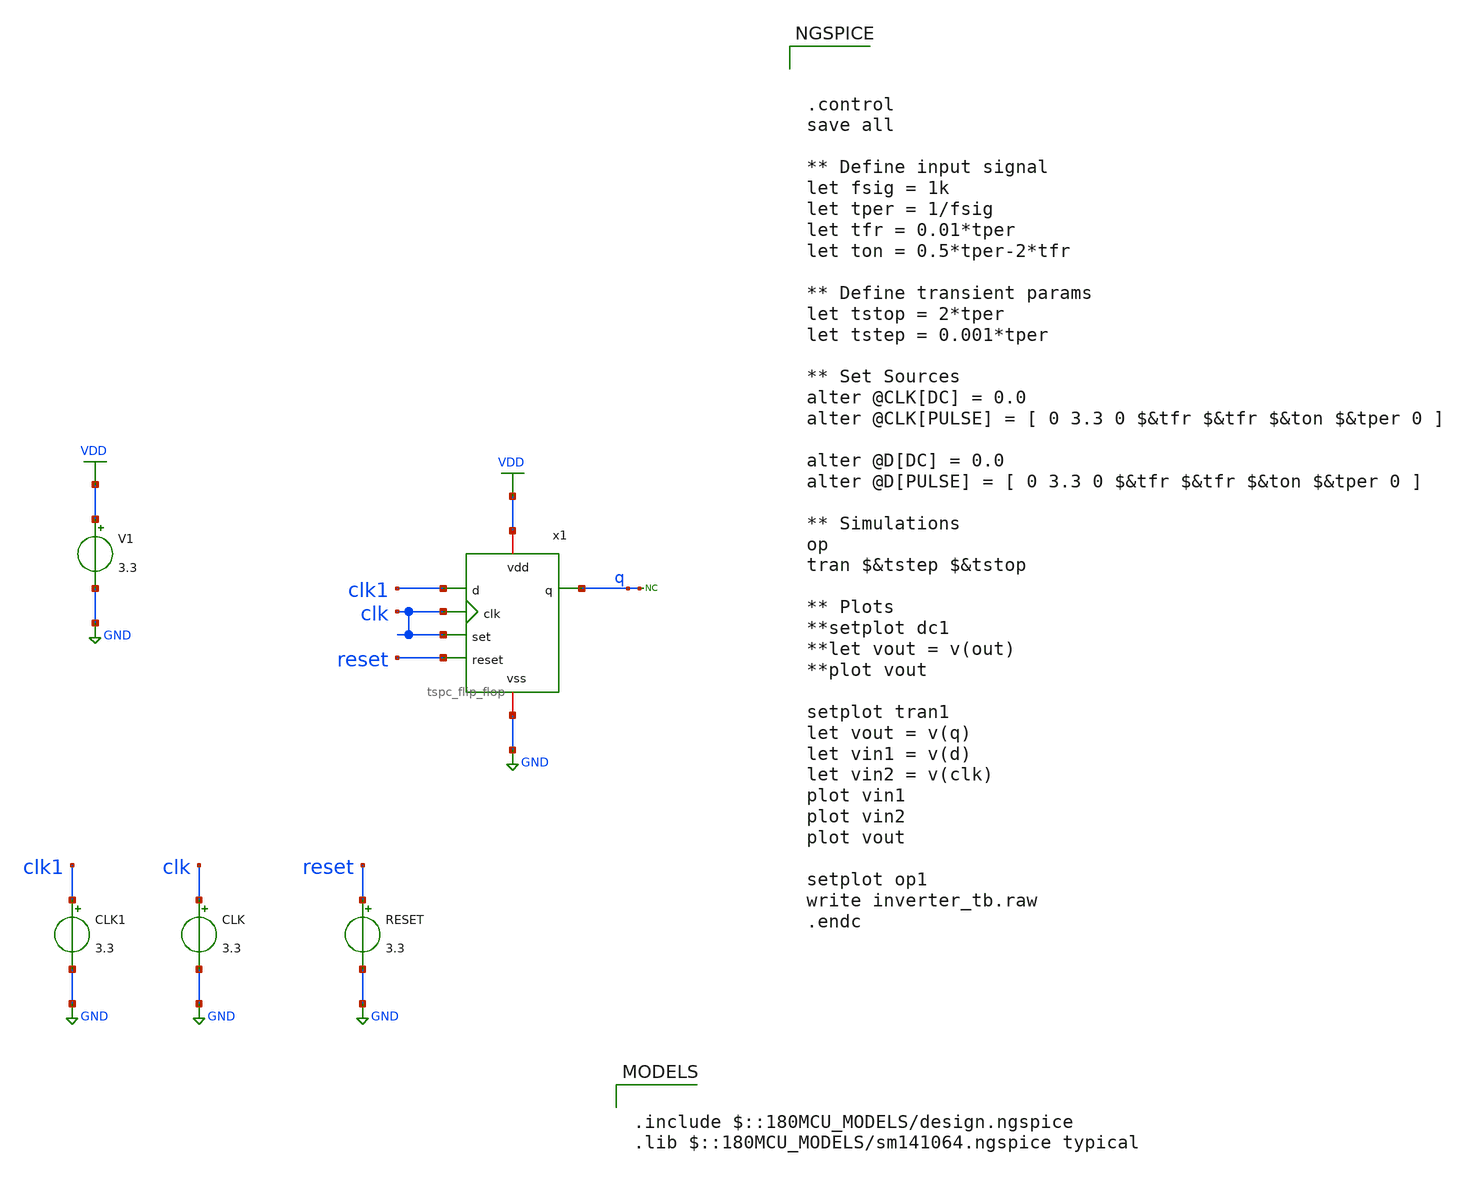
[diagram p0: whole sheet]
** sch_path: designs/libs/tspc_flip_flop/tspc_flip_flop_tb.sch
**.subckt tspc_flip_flop_tb
x1 VDD GND clk1 clk clk reset q tspc_flip_flop
V1 VDD GND 3.3
CLK clk GND 3.3
RESET reset GND 3.3
* noconn q
CLK1 clk1 GND 3.3
**** begin user architecture code

.include $::180MCU_MODELS/design.ngspice
.lib $::180MCU_MODELS/sm141064.ngspice typical




.control
save all

** Define input signal
let fsig = 1k
let tper = 1/fsig
let tfr = 0.01*tper
let ton = 0.5*tper-2*tfr

** Define transient params
let tstop = 2*tper
let tstep = 0.001*tper

** Set Sources
alter @CLK[DC] = 0.0
alter @CLK[PULSE] = [ 0 3.3 0 $&tfr $&tfr $&ton $&tper 0 ]

alter @D[DC] = 0.0
alter @D[PULSE] = [ 0 3.3 0 $&tfr $&tfr $&ton $&tper 0 ]

** Simulations
op
tran $&tstep $&tstop

** Plots
**setplot dc1
**let vout = v(out)
**plot vout

setplot tran1
let vout = v(q)
let vin1 = v(d)
let vin2 = v(clk)
plot vin1
plot vin2
plot vout

setplot op1
write inverter_tb.raw
.endc


**** end user architecture code
**.ends

* expanding   symbol:  libs/tspc_flip_flop/tspc_flip_flop.sym # of pins=7
** sym_path: designs/libs/tspc_flip_flop/tspc_flip_flop.sym
** sch_path: designs/libs/tspc_flip_flop/tspc_flip_flop.sch
.subckt tspc_flip_flop vdd vss d clk set reset q
*.iopin vdd
*.iopin vss
*.ipin d
*.ipin clk
*.ipin set
*.ipin reset
*.opin q
XM1 net2 d vss vss nfet_03v3 L=0.28u W=0.22u nf=1 ad='int((nf+1)/2) * W/nf * 0.18u' as='int((nf+2)/2) * W/nf * 0.18u'
+ pd='2*int((nf+1)/2) * (W/nf + 0.18u)' ps='2*int((nf+2)/2) * (W/nf + 0.18u)' nrd='0.18u / W' nrs='0.18u / W'
+ sa=0 sb=0 sd=0 m=1
XM2 net2 clk net1 net1 pfet_03v3 L=0.28u W=0.22u nf=1 ad='int((nf+1)/2) * W/nf * 0.18u' as='int((nf+2)/2) * W/nf * 0.18u'
+ pd='2*int((nf+1)/2) * (W/nf + 0.18u)' ps='2*int((nf+2)/2) * (W/nf + 0.18u)' nrd='0.18u / W' nrs='0.18u / W'
+ sa=0 sb=0 sd=0 m=1
XM3 net1 d vdd vdd pfet_03v3 L=0.28u W=0.22u nf=1 ad='int((nf+1)/2) * W/nf * 0.18u' as='int((nf+2)/2) * W/nf * 0.18u'
+ pd='2*int((nf+1)/2) * (W/nf + 0.18u)' ps='2*int((nf+2)/2) * (W/nf + 0.18u)' nrd='0.18u / W' nrs='0.18u / W'
+ sa=0 sb=0 sd=0 m=1
XM4 net3 clk vdd vdd pfet_03v3 L=0.28u W=0.22u nf=1 ad='int((nf+1)/2) * W/nf * 0.18u' as='int((nf+2)/2) * W/nf * 0.18u'
+ pd='2*int((nf+1)/2) * (W/nf + 0.18u)' ps='2*int((nf+2)/2) * (W/nf + 0.18u)' nrd='0.18u / W' nrs='0.18u / W'
+ sa=0 sb=0 sd=0 m=1
XM5 net3 net2 net4 vss nfet_03v3 L=0.28u W=0.22u nf=1 ad='int((nf+1)/2) * W/nf * 0.18u' as='int((nf+2)/2) * W/nf * 0.18u'
+ pd='2*int((nf+1)/2) * (W/nf + 0.18u)' ps='2*int((nf+2)/2) * (W/nf + 0.18u)' nrd='0.18u / W' nrs='0.18u / W'
+ sa=0 sb=0 sd=0 m=1
XM6 net4 clk vss vss nfet_03v3 L=0.28u W=0.22u nf=1 ad='int((nf+1)/2) * W/nf * 0.18u' as='int((nf+2)/2) * W/nf * 0.18u'
+ pd='2*int((nf+1)/2) * (W/nf + 0.18u)' ps='2*int((nf+2)/2) * (W/nf + 0.18u)' nrd='0.18u / W' nrs='0.18u / W'
+ sa=0 sb=0 sd=0 m=1
XM7 net7 net3 vss vss nfet_03v3 L=0.28u W=0.22u nf=1 ad='int((nf+1)/2) * W/nf * 0.18u' as='int((nf+2)/2) * W/nf * 0.18u'
+ pd='2*int((nf+1)/2) * (W/nf + 0.18u)' ps='2*int((nf+2)/2) * (W/nf + 0.18u)' nrd='0.18u / W' nrs='0.18u / W'
+ sa=0 sb=0 sd=0 m=1
XM8 net5 clk net7 vss nfet_03v3 L=0.28u W=0.22u nf=1 ad='int((nf+1)/2) * W/nf * 0.18u' as='int((nf+2)/2) * W/nf * 0.18u'
+ pd='2*int((nf+1)/2) * (W/nf + 0.18u)' ps='2*int((nf+2)/2) * (W/nf + 0.18u)' nrd='0.18u / W' nrs='0.18u / W'
+ sa=0 sb=0 sd=0 m=1
XM9 net5 set net6 net6 pfet_03v3 L=0.28u W=0.22u nf=1 ad='int((nf+1)/2) * W/nf * 0.18u' as='int((nf+2)/2) * W/nf * 0.18u'
+ pd='2*int((nf+1)/2) * (W/nf + 0.18u)' ps='2*int((nf+2)/2) * (W/nf + 0.18u)' nrd='0.18u / W' nrs='0.18u / W'
+ sa=0 sb=0 sd=0 m=1
XM10 net6 net3 vdd vdd pfet_03v3 L=0.28u W=0.22u nf=1 ad='int((nf+1)/2) * W/nf * 0.18u' as='int((nf+2)/2) * W/nf * 0.18u'
+ pd='2*int((nf+1)/2) * (W/nf + 0.18u)' ps='2*int((nf+2)/2) * (W/nf + 0.18u)' nrd='0.18u / W' nrs='0.18u / W'
+ sa=0 sb=0 sd=0 m=1
XM11 net5 reset vdd vdd pfet_03v3 L=0.28u W=0.22u nf=1 ad='int((nf+1)/2) * W/nf * 0.18u' as='int((nf+2)/2) * W/nf * 0.18u'
+ pd='2*int((nf+1)/2) * (W/nf + 0.18u)' ps='2*int((nf+2)/2) * (W/nf + 0.18u)' nrd='0.18u / W' nrs='0.18u / W'
+ sa=0 sb=0 sd=0 m=1
XM12 net5 set vss vss nfet_03v3 L=0.28u W=0.22u nf=1 ad='int((nf+1)/2) * W/nf * 0.18u' as='int((nf+2)/2) * W/nf * 0.18u'
+ pd='2*int((nf+1)/2) * (W/nf + 0.18u)' ps='2*int((nf+2)/2) * (W/nf + 0.18u)' nrd='0.18u / W' nrs='0.18u / W'
+ sa=0 sb=0 sd=0 m=1
XM13 q net5 vdd vdd pfet_03v3 L=0.28u W=0.22u nf=1 ad='int((nf+1)/2) * W/nf * 0.18u' as='int((nf+2)/2) * W/nf * 0.18u'
+ pd='2*int((nf+1)/2) * (W/nf + 0.18u)' ps='2*int((nf+2)/2) * (W/nf + 0.18u)' nrd='0.18u / W' nrs='0.18u / W'
+ sa=0 sb=0 sd=0 m=1
XM14 q net5 vss vss nfet_03v3 L=0.28u W=0.22u nf=1 ad='int((nf+1)/2) * W/nf * 0.18u' as='int((nf+2)/2) * W/nf * 0.18u'
+ pd='2*int((nf+1)/2) * (W/nf + 0.18u)' ps='2*int((nf+2)/2) * (W/nf + 0.18u)' nrd='0.18u / W' nrs='0.18u / W'
+ sa=0 sb=0 sd=0 m=1
.ends

.GLOBAL GND
.GLOBAL VDD
.end
